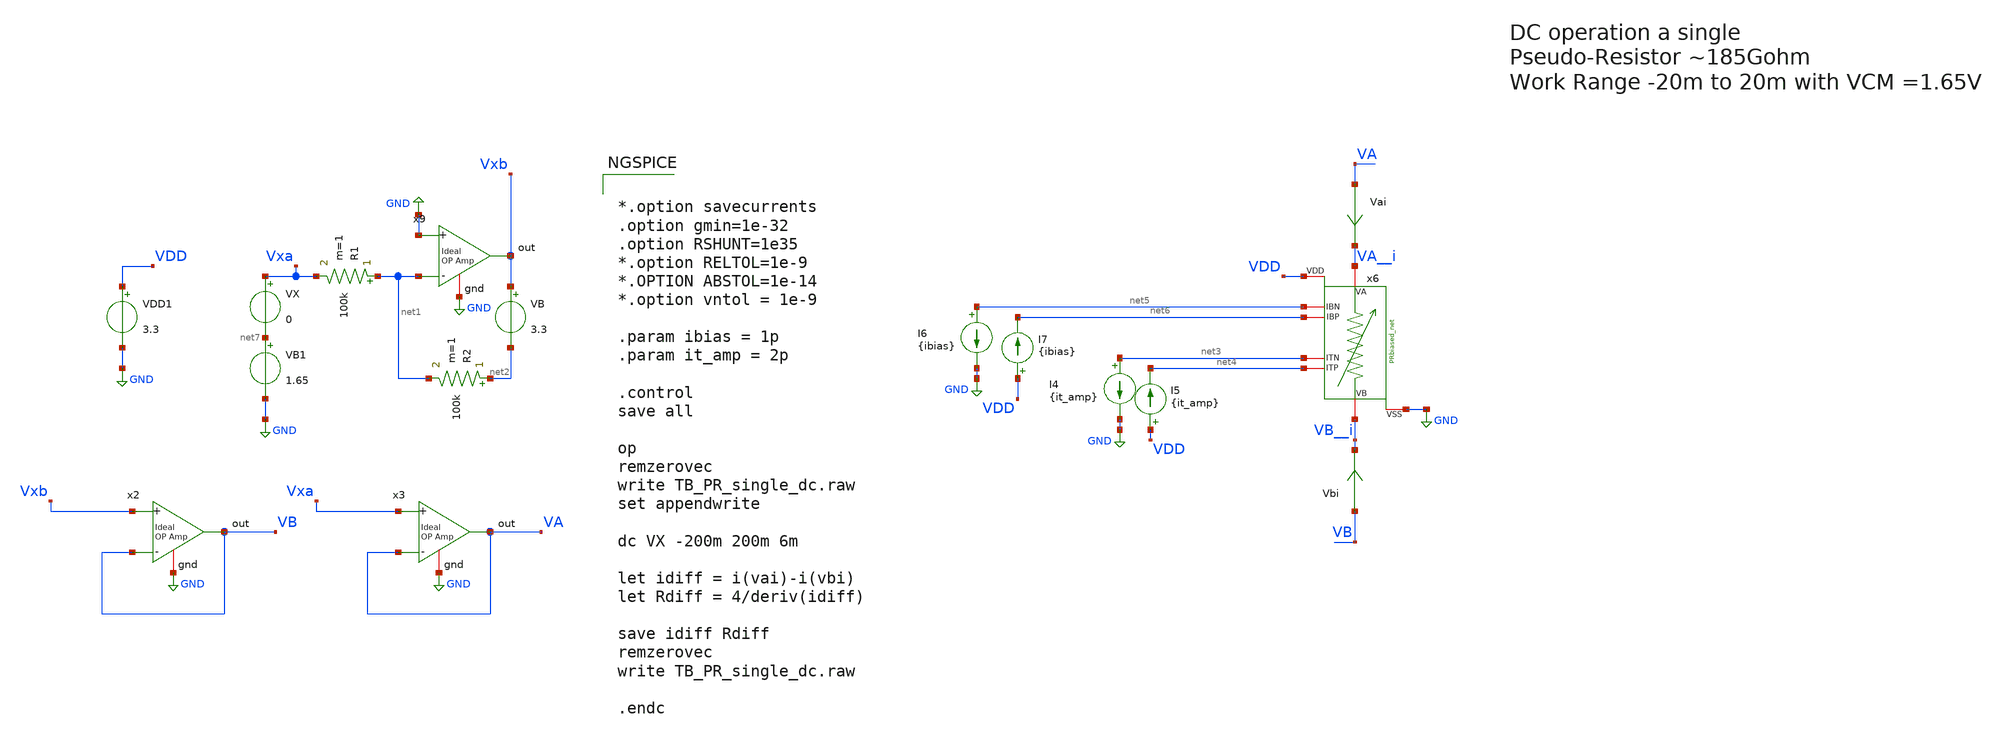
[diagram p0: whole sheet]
** sch_path: TIA/PseudoResistor/TB_PR_single_dc.sch
**.subckt TB_PR_single_dc
VDD1 VDD GND 3.3
VX Vxa net7 0
VB Vxb net2 3.3
R1 net1 Vxa 100k m=1
R2 net2 net1 100k m=1
VB1 net7 GND 1.65
x2 VB Vxb VB GND ampOp_ideal
x3 VA Vxa VA GND ampOp_ideal
x9 Vxb GND net1 GND ampOp_ideal
x6 VA__i VB__i net5 net6 net3 net4 VDD GND PRbiased_net
I4 net3 GND {it_amp}
I5 VDD net4 {it_amp}
I6 net5 GND {ibias}
I7 VDD net6 {ibias}
Vai VA VA__i 0
.save i(vai)
Vbi VB VB__i 0
.save i(vbi)
**** begin user architecture code

.include $::180MCU_MODELS/design.ngspice
.lib $::180MCU_MODELS/sm141064.ngspice typical

*.include /home/gmaranhao/Desktop/gf180_work/TIA/PseudoResistor/layout/spice/PR_net_pex.spice

*.include /home/gmaranhao/Desktop/gf180_work/TIA/PseudoResistor/layout/spice/PR_pfets_pex.spice
*.include /home/gmaranhao/Desktop/gf180_work/TIA/PseudoResistor/layout/spice/PR_nfets_pex.spice

*.subckt PR_net VSS VC VG_N IB_N VDD VB VA IB_P VG_P
*X1 0 VC vg_n ib_n VDD VB__i VA__i ib_p vg_p PR_net

*.subckt PR_nfets VD2 VG VC VS2 VS1 VD1 VB
*X2 VC_A vg_n VC VC_B ib_n VDD 0 PR_nfets

*   PR_pfets VS2_A VG VS2_B VC_A VC_B VS1 VD1 VB
*X3 VA__i vg_p VB__i VC_A VC_B 0 ib_p VDD PR_pfets





*.option savecurrents
.option gmin=1e-32
.option RSHUNT=1e35
*.option RELTOL=1e-9
*.OPTION ABSTOL=1e-14
*.option vntol = 1e-9

.param ibias = 1p
.param it_amp = 2p

.control
save all

op
remzerovec
write TB_PR_single_dc.raw
set appendwrite

dc VX -200m 200m 6m

let idiff = i(vai)-i(vbi)
let Rdiff = 4/deriv(idiff)

save idiff Rdiff
remzerovec
write TB_PR_single_dc.raw

.endc


**** end user architecture code
**.ends
.GLOBAL GND
.end
